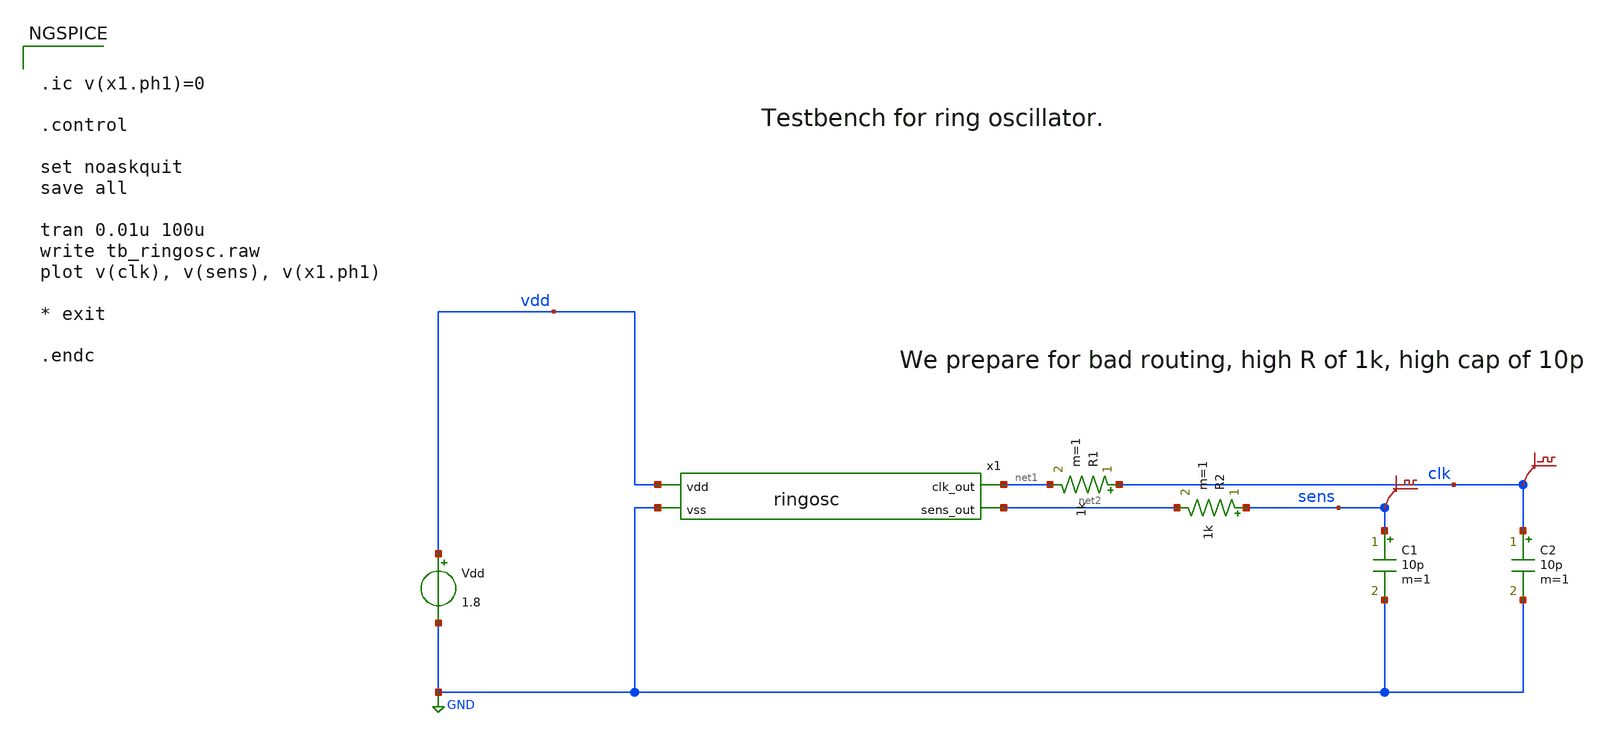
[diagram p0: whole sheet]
** sch_path: xschem/tb_ringosc.sch
**.subckt tb_ringosc
Vdd vdd GND 1.8
x1 vdd net1 net2 GND ringosc
C1 sens GND 10p m=1
C2 clk GND 10p m=1
.save v(clk)
.save v(sens)
R1 clk net1 1k m=1
R2 sens net2 1k m=1
**** begin user architecture code
 ** manual skywater pdks install (with patches applied)
* .lib $::SKYWATER_MODELS/models/sky130.lib.spice tt

** opencircuitdesign pdks install
.lib $::SKYWATER_MODELS/sky130.lib.spice.tt.red tt

.param mc_mm_switch=0
.param mc_pr_switch=0



.ic v(x1.ph1)=0

.control

set noaskquit
save all

tran 0.01u 100u
write tb_ringosc.raw
plot v(clk), v(sens), v(x1.ph1)

* exit

.endc


**** end user architecture code
**.ends

* expanding   symbol:  ringosc.sym # of pins=4
** sym_path: xschem/ringosc.sym
** sch_path: xschem/ringosc.sch
.subckt ringosc vdd clk_out sens_out vss
*.ipin vdd
*.ipin vss
*.opin clk_out
*.opin sens_out
.save v(ph1)
.save v(ph2)
.save v(ph3)
x1 vdd ph1 ph2 vss ringosc_delay
x2 vdd ph2 ph3 vss ringosc_delay
x3 vdd ph3 ph1 vss ringosc_delay
x4 vdd ph1 net2 vss ringosc_buf
x5 vdd ph2 net3 vss ringosc_buf
x6 vdd ph3 clk_out vss ringosc_buf
* noconn #net2
* noconn #net3
XR10 sens_out vdd vss sky130_fd_pr__res_xhigh_po_0p35 L=1.75 mult=1 m=1
XR1 net1 sens_out vss sky130_fd_pr__res_xhigh_po_0p35 L=1.75 mult=1 m=1
XR2 vss net1 vss sky130_fd_pr__res_xhigh_po_0p35 L=1.75 mult=1 m=1
.ends


* expanding   symbol:  ringosc_delay.sym # of pins=4
** sym_path: xschem/ringosc_delay.sym
** sch_path: xschem/ringosc_delay.sch
.subckt ringosc_delay vdd in out vss
*.ipin vdd
*.ipin vss
*.ipin in
*.opin out
XM1 out in vdd vdd sky130_fd_pr__pfet_01v8 L=10 W=0.5 nf=1 ad='int((nf+1)/2) * W/nf * 0.29' as='int((nf+2)/2) * W/nf * 0.29'
+ pd='2*int((nf+1)/2) * (W/nf + 0.29)' ps='2*int((nf+2)/2) * (W/nf + 0.29)' nrd='0.29 / W' nrs='0.29 / W'
+ sa=0 sb=0 sd=0 mult=1 m=1
XM2 out in net1 vss sky130_fd_pr__nfet_01v8 L=10 W=0.5 nf=1 ad='int((nf+1)/2) * W/nf * 0.29' as='int((nf+2)/2) * W/nf * 0.29'
+ pd='2*int((nf+1)/2) * (W/nf + 0.29)' ps='2*int((nf+2)/2) * (W/nf + 0.29)' nrd='0.29 / W' nrs='0.29 / W'
+ sa=0 sb=0 sd=0 mult=1 m=1
XM4 vss out vss vss sky130_fd_pr__nfet_01v8 L=2 W=10 nf=1 ad='int((nf+1)/2) * W/nf * 0.29' as='int((nf+2)/2) * W/nf * 0.29'
+ pd='2*int((nf+1)/2) * (W/nf + 0.29)' ps='2*int((nf+2)/2) * (W/nf + 0.29)' nrd='0.29 / W' nrs='0.29 / W'
+ sa=0 sb=0 sd=0 mult=1 m=1
XM5 vdd out vdd vdd sky130_fd_pr__pfet_01v8 L=2 W=10 nf=1 ad='int((nf+1)/2) * W/nf * 0.29' as='int((nf+2)/2) * W/nf * 0.29'
+ pd='2*int((nf+1)/2) * (W/nf + 0.29)' ps='2*int((nf+2)/2) * (W/nf + 0.29)' nrd='0.29 / W' nrs='0.29 / W'
+ sa=0 sb=0 sd=0 mult=1 m=1
XM3 net1 in vss vss sky130_fd_pr__nfet_01v8 L=10 W=0.5 nf=1 ad='int((nf+1)/2) * W/nf * 0.29' as='int((nf+2)/2) * W/nf * 0.29'
+ pd='2*int((nf+1)/2) * (W/nf + 0.29)' ps='2*int((nf+2)/2) * (W/nf + 0.29)' nrd='0.29 / W' nrs='0.29 / W'
+ sa=0 sb=0 sd=0 mult=1 m=1
.ends


* expanding   symbol:  ringosc_buf.sym # of pins=4
** sym_path: xschem/ringosc_buf.sym
** sch_path: xschem/ringosc_buf.sch
.subckt ringosc_buf vdd in out vss
*.ipin vdd
*.ipin vss
*.ipin in
*.opin out
XM2 out in vss vss sky130_fd_pr__nfet_01v8 L=0.5 W=10 nf=1 ad='int((nf+1)/2) * W/nf * 0.29' as='int((nf+2)/2) * W/nf * 0.29'
+ pd='2*int((nf+1)/2) * (W/nf + 0.29)' ps='2*int((nf+2)/2) * (W/nf + 0.29)' nrd='0.29 / W' nrs='0.29 / W'
+ sa=0 sb=0 sd=0 mult=1 m=1
XM8 out in vdd vdd sky130_fd_pr__pfet_01v8 L=0.5 W=10 nf=1 ad='int((nf+1)/2) * W/nf * 0.29' as='int((nf+2)/2) * W/nf * 0.29'
+ pd='2*int((nf+1)/2) * (W/nf + 0.29)' ps='2*int((nf+2)/2) * (W/nf + 0.29)' nrd='0.29 / W' nrs='0.29 / W'
+ sa=0 sb=0 sd=0 mult=1 m=1
XM1 out in vdd vdd sky130_fd_pr__pfet_01v8 L=0.5 W=10 nf=1 ad='int((nf+1)/2) * W/nf * 0.29' as='int((nf+2)/2) * W/nf * 0.29'
+ pd='2*int((nf+1)/2) * (W/nf + 0.29)' ps='2*int((nf+2)/2) * (W/nf + 0.29)' nrd='0.29 / W' nrs='0.29 / W'
+ sa=0 sb=0 sd=0 mult=1 m=1
.ends

.GLOBAL GND
.end
